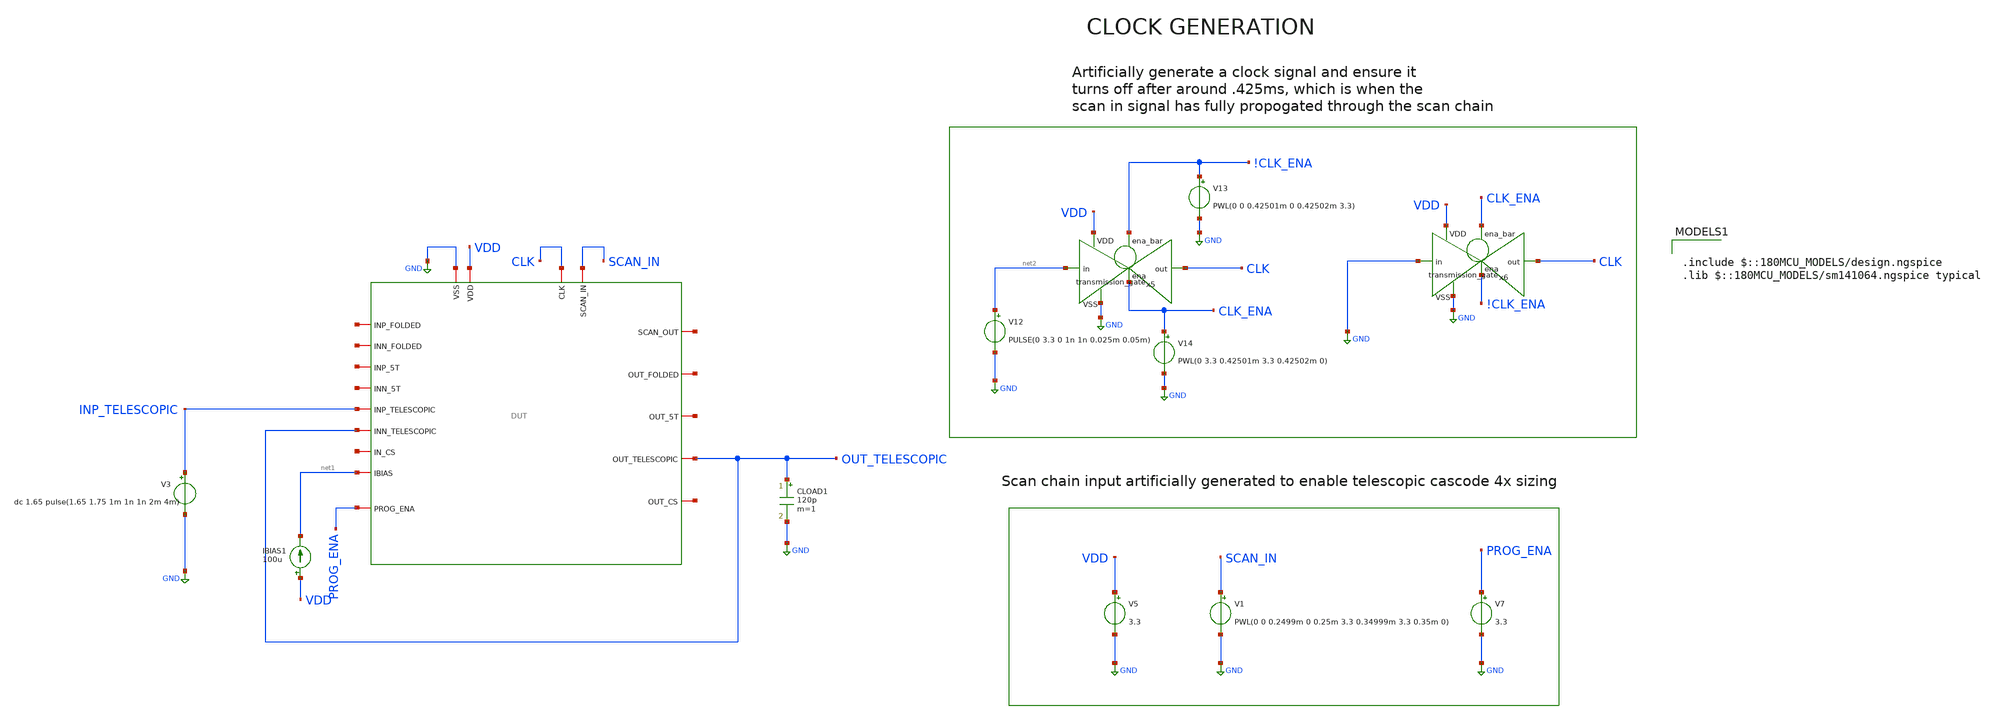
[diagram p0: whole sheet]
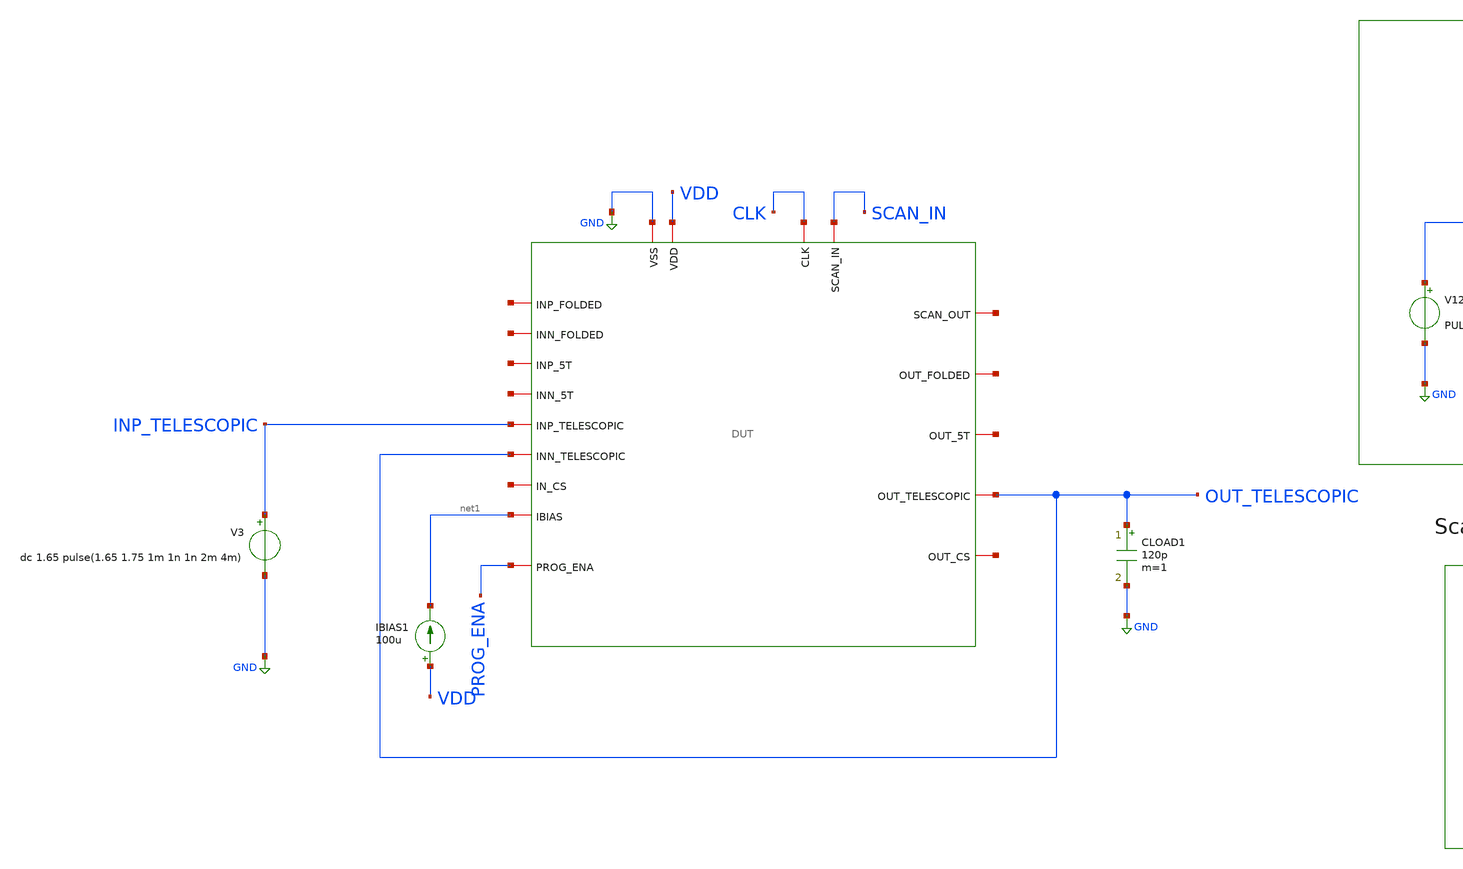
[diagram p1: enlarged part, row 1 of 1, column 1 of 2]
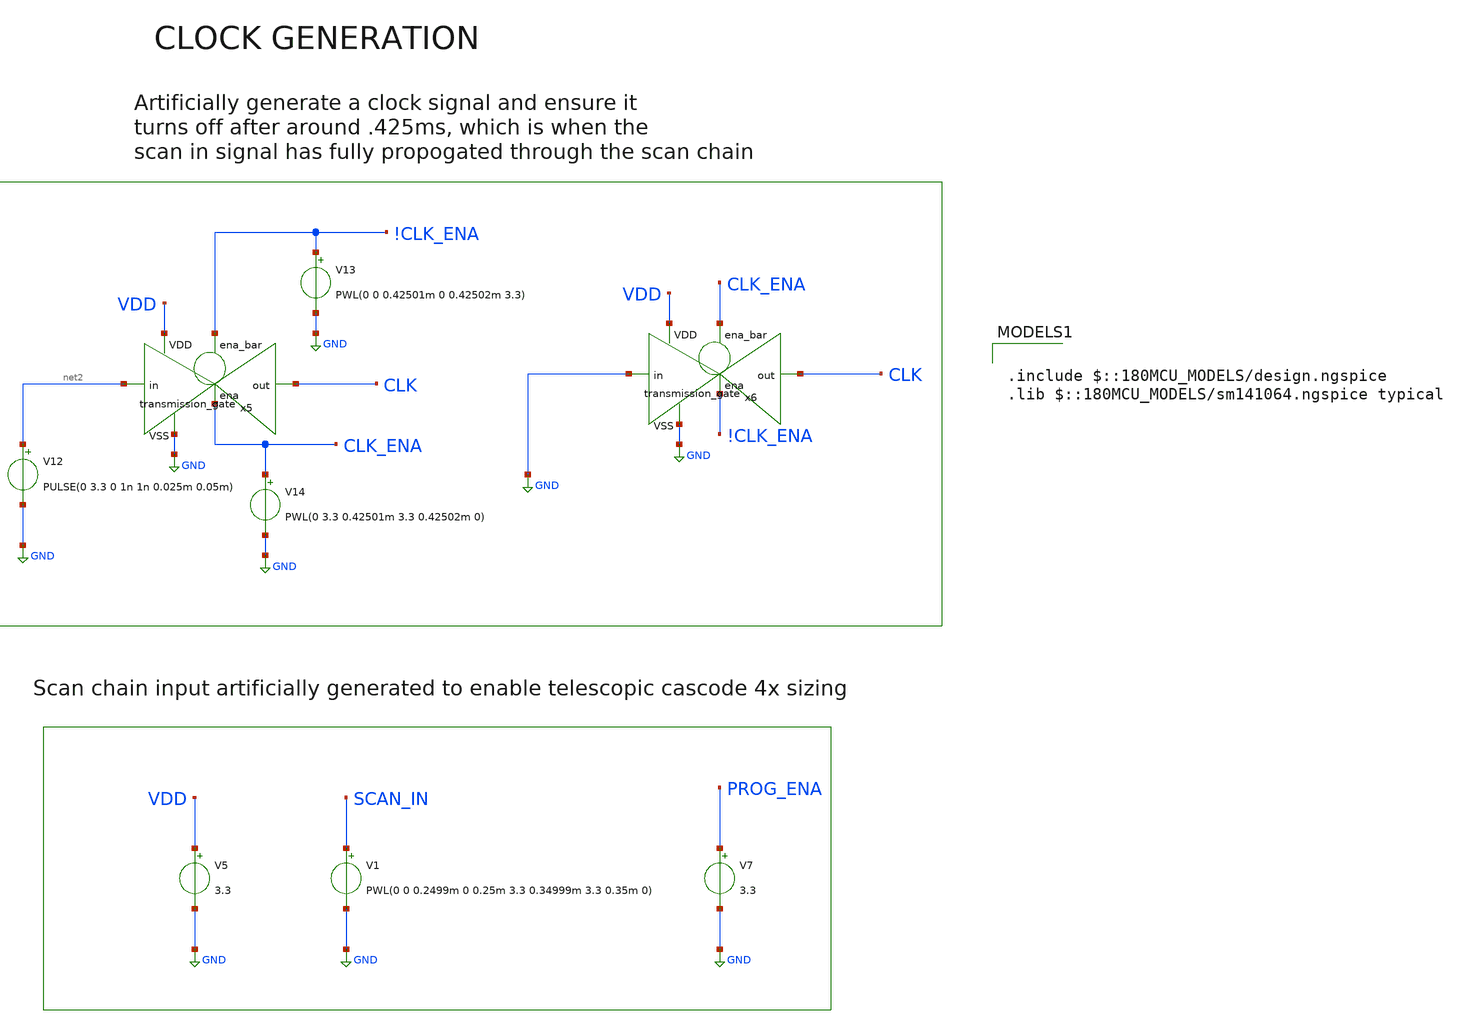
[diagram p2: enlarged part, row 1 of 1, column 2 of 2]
** sch_path: designs/libs/verification/ota_telescopic/4x/sr.sch
**.subckt sr
x2 CLK net3 SCAN_IN GND VDD net4 net5 net6 net1 net7 net8 net9 INP_TELESCOPIC OUT_TELESCOPIC net10
+ net11 OUT_TELESCOPIC PROG_ENA DUT
CLOAD1 OUT_TELESCOPIC GND 120p m=1
V3 INP_TELESCOPIC GND dc 1.65 pulse(1.65 1.75 1m 1n 1n 2m 4m)
IBIAS1 VDD net1 100u
V5 VDD GND 3.3
V7 PROG_ENA GND 3.3
V12 net2 GND PULSE(0 3.3 0 1n 1n 0.025m 0.05m)
x5 !CLK_ENA VDD CLK net2 GND CLK_ENA transmission_gate
V13 !CLK_ENA GND PWL(0 0 0.42501m 0 0.42502m 3.3)
V14 CLK_ENA GND PWL(0 3.3 0.42501m 3.3 0.42502m 0)
x6 CLK_ENA VDD CLK GND GND !CLK_ENA transmission_gate
V1 SCAN_IN GND PWL(0 0 0.2499m 0 0.25m 3.3 0.34999m 3.3 0.35m 0)
**** begin user architecture code

.include $::180MCU_MODELS/design.ngspice
.lib $::180MCU_MODELS/sm141064.ngspice typical



.control
tran 1u 5m

plot v(out_telescopic) v(inp_telescopic)

meas tran v_before find v(out_telescopic) at=0.99m
meas tran v_after find v(out_telescopic) at=2.5m
print t_20
print t_80
let delta = v_after - v_before
let t20_val = v_before + 0.2 * delta
let t80_val = v_before + 0.8 * delta

meas tran t_20 when v(out_telescopic) = t20_val rise = 1 td=.99m
meas tran t_80 when v(out_telescopic) = t80_val rise = 1 td=.99m
let sr_rise = delta / (t_80 - t_20)
print sr_rise

meas tran t_20f when v(out_telescopic) = t80_val fall = 1 td=.99m
meas tran t_80f when v(out_telescopic) = t20_val fall = 1 td=.99m
let sr_fall = delta / (t_80f - t_20f)
print sr_fall

meas tran vpeak max v(out_telescopic) from=1m to=3m
let overshoot = (vpeak - v_after) / delta * 100
print overshoot

meas tran t_settle when v(out_telescopic) = v_after td = 1m rise = 1
let settling = t_settle - 1m
print settling

print v_before v_after delta
.endc


**** end user architecture code
**.ends
.GLOBAL GND
.end
